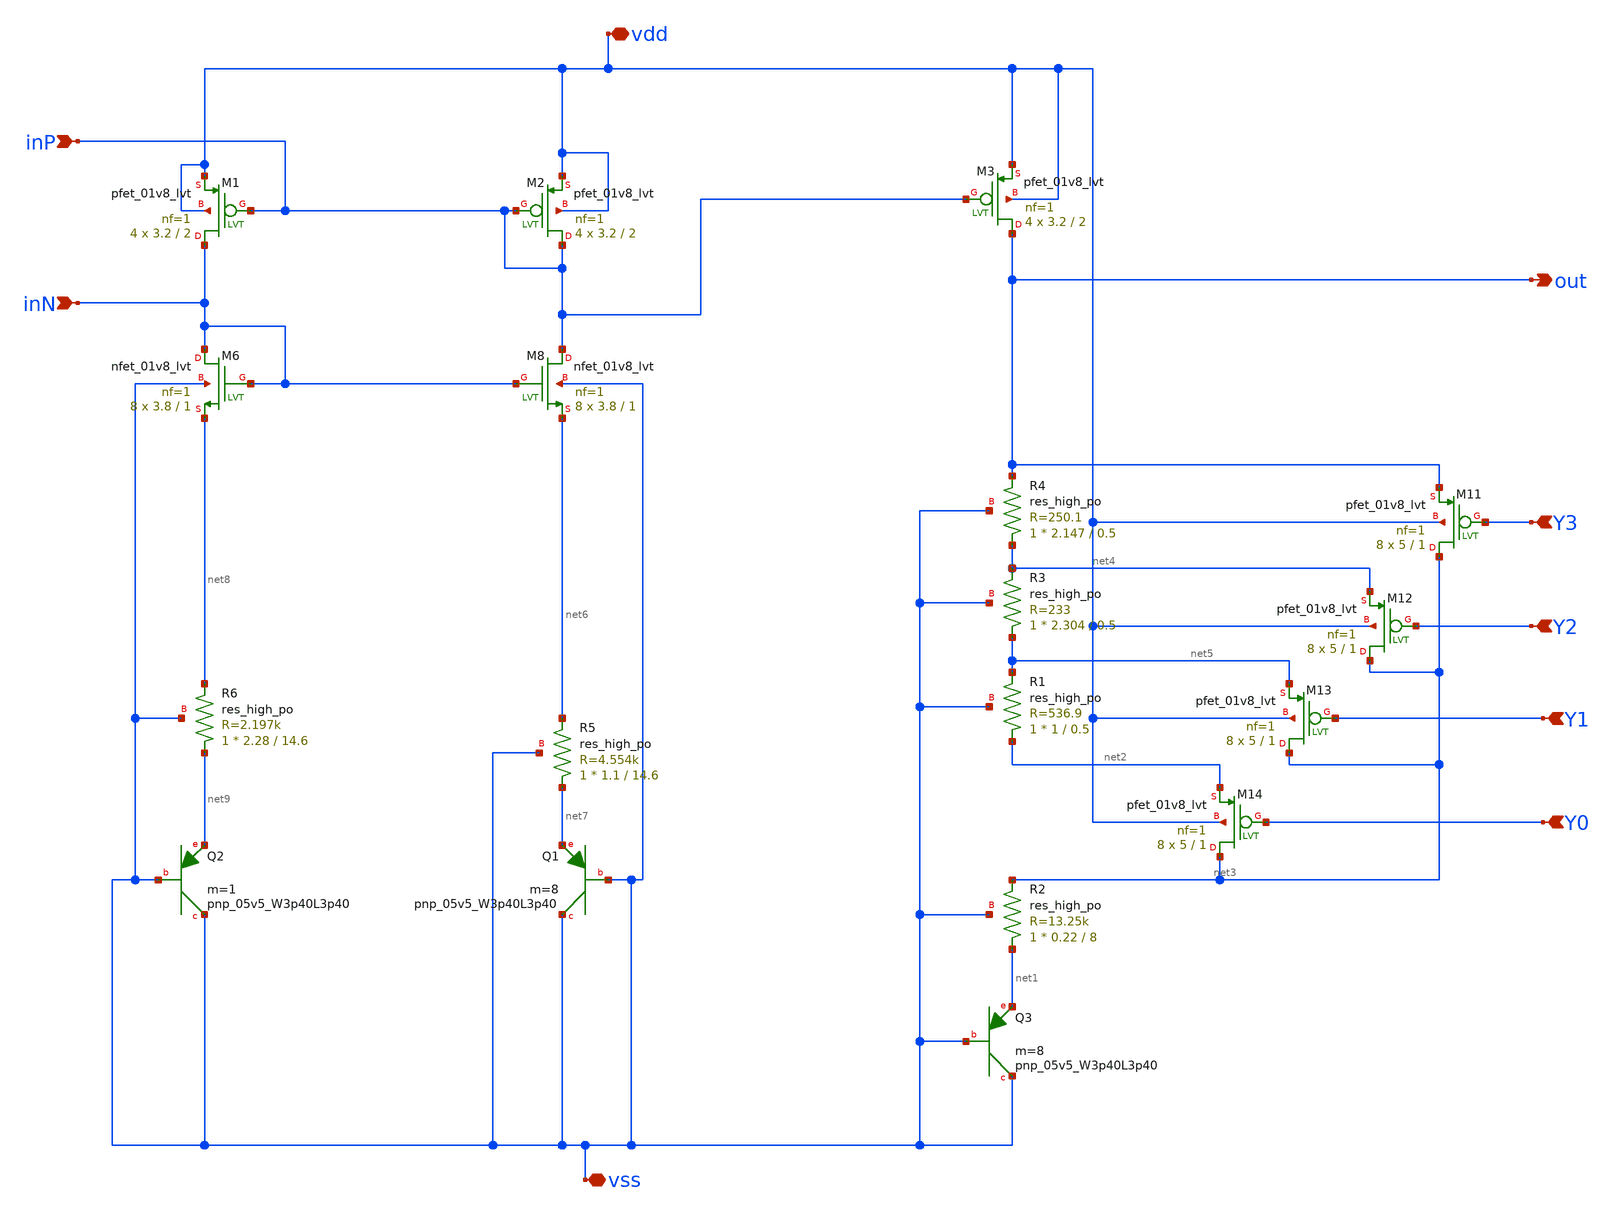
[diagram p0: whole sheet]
** sch_path: BGR_coreAndVrefBranch.sch
**.subckt BGR_coreAndVrefBranch out vss Y3 Y2 Y1 Y0 vdd inP inN
*.opin out
*.iopin vss
*.ipin Y3
*.ipin Y2
*.ipin Y1
*.ipin Y0
*.iopin vdd
*.ipin inP
*.ipin inN
XM3 out inP vdd vdd sky130_fd_pr__pfet_01v8_lvt L=2 W=3.2 nf=1 ad='int((1 + 1)/2) * 3.2 / 1 * 0.29' as='int((1 + 2)/2) * 3.2 / 1 * 0.29'
+ pd='2*int((1 + 1)/2) * (3.2 / 1 + 0.29)' ps='2*int((1 + 2)/2) * (3.2 / 1 + 0.29)' nrd='0.29 / 3.2 ' nrs='0.29 / 3.2 '
+ sa=0 sb=0 sd=0 mult=4 m=4
XQ3 vss vss net1 sky130_fd_pr__pnp_05v5_W3p40L3p40 m=8
XR2 net1 net3 vss sky130_fd_pr__res_high_po W=0.22 L=8 mult=1 m=1
XM11 net3 Y3 out vdd sky130_fd_pr__pfet_01v8_lvt L=1 W=5 nf=1 ad='int((1 + 1)/2) * 5 / 1 * 0.29' as='int((1 + 2)/2) * 5 / 1 * 0.29'
+ pd='2*int((1 + 1)/2) * (5 / 1 + 0.29)' ps='2*int((1 + 2)/2) * (5 / 1 + 0.29)' nrd='0.29 / 5 ' nrs='0.29 / 5 '
+ sa=0 sb=0 sd=0 mult=8 m=8
XM12 net3 Y2 net4 vdd sky130_fd_pr__pfet_01v8_lvt L=1 W=5 nf=1 ad='int((1 + 1)/2) * 5 / 1 * 0.29' as='int((1 + 2)/2) * 5 / 1 * 0.29'
+ pd='2*int((1 + 1)/2) * (5 / 1 + 0.29)' ps='2*int((1 + 2)/2) * (5 / 1 + 0.29)' nrd='0.29 / 5 ' nrs='0.29 / 5 '
+ sa=0 sb=0 sd=0 mult=8 m=8
XM13 net3 Y1 net5 vdd sky130_fd_pr__pfet_01v8_lvt L=1 W=5 nf=1 ad='int((1 + 1)/2) * 5 / 1 * 0.29' as='int((1 + 2)/2) * 5 / 1 * 0.29'
+ pd='2*int((1 + 1)/2) * (5 / 1 + 0.29)' ps='2*int((1 + 2)/2) * (5 / 1 + 0.29)' nrd='0.29 / 5 ' nrs='0.29 / 5 '
+ sa=0 sb=0 sd=0 mult=8 m=8
XM14 net3 Y0 net2 vdd sky130_fd_pr__pfet_01v8_lvt L=1 W=5 nf=1 ad='int((1 + 1)/2) * 5 / 1 * 0.29' as='int((1 + 2)/2) * 5 / 1 * 0.29'
+ pd='2*int((1 + 1)/2) * (5 / 1 + 0.29)' ps='2*int((1 + 2)/2) * (5 / 1 + 0.29)' nrd='0.29 / 5 ' nrs='0.29 / 5 '
+ sa=0 sb=0 sd=0 mult=8 m=8
XR1 net2 net5 vss sky130_fd_pr__res_high_po W=1 L=0.5 mult=1 m=1
XR3 net5 net4 vss sky130_fd_pr__res_high_po W=2.304 L=0.5 mult=1 m=1
XR4 net4 out vss sky130_fd_pr__res_high_po W=2.147 L=0.5 mult=1 m=1
XM6 inN inN net8 vss sky130_fd_pr__nfet_01v8_lvt L=1 W=3.8 nf=1 ad='int((1 + 1)/2) * 3.8 / 1 * 0.29'
+ as='int((1 + 2)/2) * 3.8 / 1 * 0.29' pd='2*int((1 + 1)/2) * (3.8 / 1 + 0.29)' ps='2*int((1 + 2)/2) * (3.8 / 1 + 0.29)'
+ nrd='0.29 / 3.8 ' nrs='0.29 / 3.8 ' sa=0 sb=0 sd=0 mult=8 m=8
XM1 inN inP vdd vdd sky130_fd_pr__pfet_01v8_lvt L=2 W=3.2 nf=1 ad='int((1 + 1)/2) * 3.2 / 1 * 0.29' as='int((1 + 2)/2) * 3.2 / 1 * 0.29'
+ pd='2*int((1 + 1)/2) * (3.2 / 1 + 0.29)' ps='2*int((1 + 2)/2) * (3.2 / 1 + 0.29)' nrd='0.29 / 3.2 ' nrs='0.29 / 3.2 '
+ sa=0 sb=0 sd=0 mult=4 m=4
XQ1 vss vss net7 sky130_fd_pr__pnp_05v5_W3p40L3p40 m=8
XR5 net7 net6 vss sky130_fd_pr__res_high_po W=1.1 L=14.6 mult=1 m=1
XM2 inP inP vdd vdd sky130_fd_pr__pfet_01v8_lvt L=2 W=3.2 nf=1 ad='int((1 + 1)/2) * 3.2 / 1 * 0.29' as='int((1 + 2)/2) * 3.2 / 1 * 0.29'
+ pd='2*int((1 + 1)/2) * (3.2 / 1 + 0.29)' ps='2*int((1 + 2)/2) * (3.2 / 1 + 0.29)' nrd='0.29 / 3.2 ' nrs='0.29 / 3.2 '
+ sa=0 sb=0 sd=0 mult=4 m=4
XM8 inP inN net6 vss sky130_fd_pr__nfet_01v8_lvt L=1 W=3.8 nf=1 ad='int((1 + 1)/2) * 3.8 / 1 * 0.29'
+ as='int((1 + 2)/2) * 3.8 / 1 * 0.29' pd='2*int((1 + 1)/2) * (3.8 / 1 + 0.29)' ps='2*int((1 + 2)/2) * (3.8 / 1 + 0.29)'
+ nrd='0.29 / 3.8 ' nrs='0.29 / 3.8 ' sa=0 sb=0 sd=0 mult=8 m=8
XQ2 vss vss net9 sky130_fd_pr__pnp_05v5_W3p40L3p40 m=1
XR6 net9 net8 vss sky130_fd_pr__res_high_po W=2.28 L=14.6 mult=1 m=1
**.ends
.end
